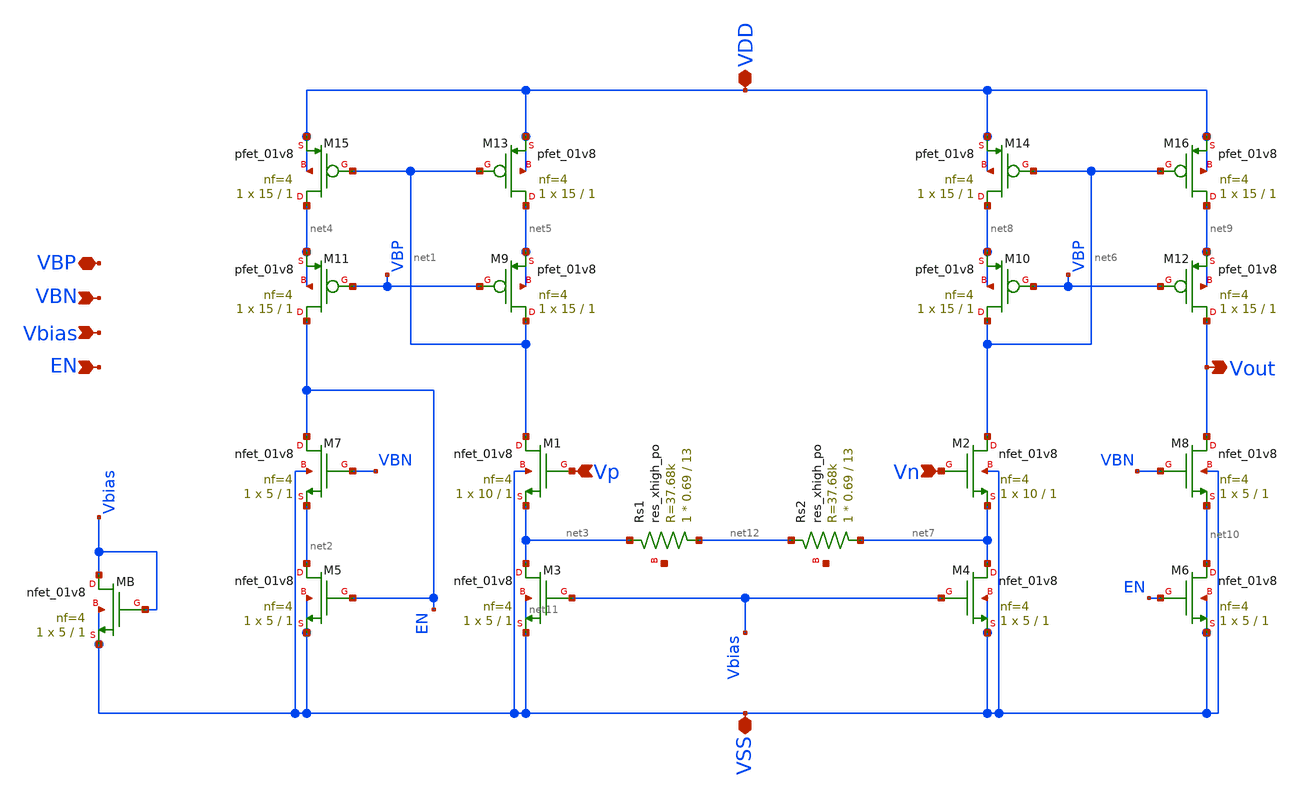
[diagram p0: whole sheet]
** sch_path: design_data/xschem/OTA.sch
**.subckt OTA Vp Vout VSS VDD Vn Vbias EN VBN VBP
*.ipin Vp
*.opin Vout
*.iopin VSS
*.iopin VDD
*.ipin Vn
*.ipin Vbias
*.ipin EN
*.ipin VBN
*.iopin VBP
XM1 net1 Vp net3 VSS sky130_fd_pr__nfet_01v8 L=1 W=10 nf=4 ad='int((nf+1)/2) * W/nf * 0.29' as='int((nf+2)/2) * W/nf * 0.29'
+ pd='2*int((nf+1)/2) * (W/nf + 0.29)' ps='2*int((nf+2)/2) * (W/nf + 0.29)' nrd='0.29 / W' nrs='0.29 / W'
+ sa=0 sb=0 sd=0 mult=1 m=1
XM13 net5 net1 VDD VDD sky130_fd_pr__pfet_01v8 L=1 W=15 nf=4 ad='int((nf+1)/2) * W/nf * 0.29' as='int((nf+2)/2) * W/nf * 0.29'
+ pd='2*int((nf+1)/2) * (W/nf + 0.29)' ps='2*int((nf+2)/2) * (W/nf + 0.29)' nrd='0.29 / W' nrs='0.29 / W'
+ sa=0 sb=0 sd=0 mult=1 m=1
XM15 net4 net1 VDD VDD sky130_fd_pr__pfet_01v8 L=1 W=15 nf=4 ad='int((nf+1)/2) * W/nf * 0.29' as='int((nf+2)/2) * W/nf * 0.29'
+ pd='2*int((nf+1)/2) * (W/nf + 0.29)' ps='2*int((nf+2)/2) * (W/nf + 0.29)' nrd='0.29 / W' nrs='0.29 / W'
+ sa=0 sb=0 sd=0 mult=1 m=1
XM7 EN VBN net2 VSS sky130_fd_pr__nfet_01v8 L=1 W=5 nf=4 ad='int((nf+1)/2) * W/nf * 0.29' as='int((nf+2)/2) * W/nf * 0.29'
+ pd='2*int((nf+1)/2) * (W/nf + 0.29)' ps='2*int((nf+2)/2) * (W/nf + 0.29)' nrd='0.29 / W' nrs='0.29 / W'
+ sa=0 sb=0 sd=0 mult=1 m=1
XM9 net1 VBP net5 net5 sky130_fd_pr__pfet_01v8 L=1 W=15 nf=4 ad='int((nf+1)/2) * W/nf * 0.29' as='int((nf+2)/2) * W/nf * 0.29'
+ pd='2*int((nf+1)/2) * (W/nf + 0.29)' ps='2*int((nf+2)/2) * (W/nf + 0.29)' nrd='0.29 / W' nrs='0.29 / W'
+ sa=0 sb=0 sd=0 mult=1 m=1
XM11 EN VBP net4 net4 sky130_fd_pr__pfet_01v8 L=1 W=15 nf=4 ad='int((nf+1)/2) * W/nf * 0.29' as='int((nf+2)/2) * W/nf * 0.29'
+ pd='2*int((nf+1)/2) * (W/nf + 0.29)' ps='2*int((nf+2)/2) * (W/nf + 0.29)' nrd='0.29 / W' nrs='0.29 / W'
+ sa=0 sb=0 sd=0 mult=1 m=1
XM3 net3 Vbias VSS net11 sky130_fd_pr__nfet_01v8 L=1 W=5 nf=4 ad='int((nf+1)/2) * W/nf * 0.29' as='int((nf+2)/2) * W/nf * 0.29'
+ pd='2*int((nf+1)/2) * (W/nf + 0.29)' ps='2*int((nf+2)/2) * (W/nf + 0.29)' nrd='0.29 / W' nrs='0.29 / W'
+ sa=0 sb=0 sd=0 mult=1 m=1
XM5 net2 EN VSS VSS sky130_fd_pr__nfet_01v8 L=1 W=5 nf=4 ad='int((nf+1)/2) * W/nf * 0.29' as='int((nf+2)/2) * W/nf * 0.29'
+ pd='2*int((nf+1)/2) * (W/nf + 0.29)' ps='2*int((nf+2)/2) * (W/nf + 0.29)' nrd='0.29 / W' nrs='0.29 / W'
+ sa=0 sb=0 sd=0 mult=1 m=1
XM8 Vout VBN net10 VSS sky130_fd_pr__nfet_01v8 L=1 W=5 nf=4 ad='int((nf+1)/2) * W/nf * 0.29' as='int((nf+2)/2) * W/nf * 0.29'
+ pd='2*int((nf+1)/2) * (W/nf + 0.29)' ps='2*int((nf+2)/2) * (W/nf + 0.29)' nrd='0.29 / W' nrs='0.29 / W'
+ sa=0 sb=0 sd=0 mult=1 m=1
XM16 net9 net6 VDD VDD sky130_fd_pr__pfet_01v8 L=1 W=15 nf=4 ad='int((nf+1)/2) * W/nf * 0.29' as='int((nf+2)/2) * W/nf * 0.29'
+ pd='2*int((nf+1)/2) * (W/nf + 0.29)' ps='2*int((nf+2)/2) * (W/nf + 0.29)' nrd='0.29 / W' nrs='0.29 / W'
+ sa=0 sb=0 sd=0 mult=1 m=1
XM14 net8 net6 VDD VDD sky130_fd_pr__pfet_01v8 L=1 W=15 nf=4 ad='int((nf+1)/2) * W/nf * 0.29' as='int((nf+2)/2) * W/nf * 0.29'
+ pd='2*int((nf+1)/2) * (W/nf + 0.29)' ps='2*int((nf+2)/2) * (W/nf + 0.29)' nrd='0.29 / W' nrs='0.29 / W'
+ sa=0 sb=0 sd=0 mult=1 m=1
XM2 net6 Vn net7 VSS sky130_fd_pr__nfet_01v8 L=1 W=10 nf=4 ad='int((nf+1)/2) * W/nf * 0.29' as='int((nf+2)/2) * W/nf * 0.29'
+ pd='2*int((nf+1)/2) * (W/nf + 0.29)' ps='2*int((nf+2)/2) * (W/nf + 0.29)' nrd='0.29 / W' nrs='0.29 / W'
+ sa=0 sb=0 sd=0 mult=1 m=1
XM12 Vout VBP net9 net9 sky130_fd_pr__pfet_01v8 L=1 W=15 nf=4 ad='int((nf+1)/2) * W/nf * 0.29' as='int((nf+2)/2) * W/nf * 0.29'
+ pd='2*int((nf+1)/2) * (W/nf + 0.29)' ps='2*int((nf+2)/2) * (W/nf + 0.29)' nrd='0.29 / W' nrs='0.29 / W'
+ sa=0 sb=0 sd=0 mult=1 m=1
XM10 net6 VBP net8 net8 sky130_fd_pr__pfet_01v8 L=1 W=15 nf=4 ad='int((nf+1)/2) * W/nf * 0.29' as='int((nf+2)/2) * W/nf * 0.29'
+ pd='2*int((nf+1)/2) * (W/nf + 0.29)' ps='2*int((nf+2)/2) * (W/nf + 0.29)' nrd='0.29 / W' nrs='0.29 / W'
+ sa=0 sb=0 sd=0 mult=1 m=1
XM6 net10 EN VSS VSS sky130_fd_pr__nfet_01v8 L=1 W=5 nf=4 ad='int((nf+1)/2) * W/nf * 0.29' as='int((nf+2)/2) * W/nf * 0.29'
+ pd='2*int((nf+1)/2) * (W/nf + 0.29)' ps='2*int((nf+2)/2) * (W/nf + 0.29)' nrd='0.29 / W' nrs='0.29 / W'
+ sa=0 sb=0 sd=0 mult=1 m=1
XM4 net7 Vbias VSS VSS sky130_fd_pr__nfet_01v8 L=1 W=5 nf=4 ad='int((nf+1)/2) * W/nf * 0.29' as='int((nf+2)/2) * W/nf * 0.29'
+ pd='2*int((nf+1)/2) * (W/nf + 0.29)' ps='2*int((nf+2)/2) * (W/nf + 0.29)' nrd='0.29 / W' nrs='0.29 / W'
+ sa=0 sb=0 sd=0 mult=1 m=1
XMB Vbias Vbias VSS VSS sky130_fd_pr__nfet_01v8 L=1 W=5 nf=4 ad='int((nf+1)/2) * W/nf * 0.29' as='int((nf+2)/2) * W/nf * 0.29'
+ pd='2*int((nf+1)/2) * (W/nf + 0.29)' ps='2*int((nf+2)/2) * (W/nf + 0.29)' nrd='0.29 / W' nrs='0.29 / W'
+ sa=0 sb=0 sd=0 mult=1 m=1
XRs1 net12 net3 net13 sky130_fd_pr__res_xhigh_po W=0.69 L=13 mult=1 m=1
XRs2 net7 net12 net14 sky130_fd_pr__res_xhigh_po W=0.69 L=13 mult=1 m=1
**** begin user architecture code
"Is Subcircuit" = YES
**** end user architecture code
**.ends
.end
